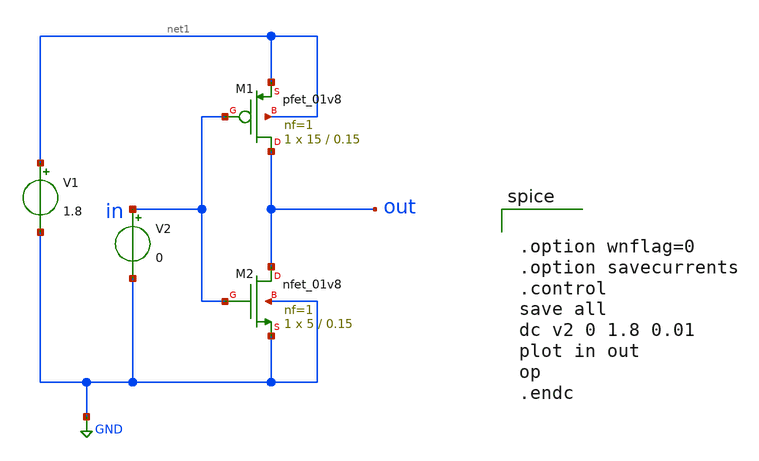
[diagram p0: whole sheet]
** sch_path: inverter_cmos.sch
**.subckt inverter_cmos
XM1 out in net1 net1 sky130_fd_pr__pfet_01v8 L=0.15 W=15 nf=1 ad='int((1 + 1)/2) * 15 / 1 * 0.29' as='int((1 + 2)/2) * 15 / 1 * 0.29'
+ pd='2*int((1 + 1)/2) * (15 / 1 + 0.29)' ps='2*int((1 + 2)/2) * (15 / 1 + 0.29)' nrd='0.29 / 15 ' nrs='0.29 / 15 '
+ sa=0 sb=0 sd=0 mult=1 m=1
XM2 out in GND GND sky130_fd_pr__nfet_01v8 L=0.15 W=5 nf=1 ad='int((1 + 1)/2) * 5 / 1 * 0.29' as='int((1 + 2)/2) * 5 / 1 * 0.29'
+ pd='2*int((1 + 1)/2) * (5 / 1 + 0.29)' ps='2*int((1 + 2)/2) * (5 / 1 + 0.29)' nrd='0.29 / 5 ' nrs='0.29 / 5 '
+ sa=0 sb=0 sd=0 mult=1 m=1
V1 net1 GND 1.8
V2 in GND 0
**** begin user architecture code
 .lib /foss/pdks/sky130A/libs.tech/combined/sky130.lib.spice tt

.param mc_mm_switch=0
.param mc_pr_switch=1



.option wnflag=0
.option savecurrents
.control
save all
dc v2 0 1.8 0.01
plot in out
op
.endc


**** end user architecture code
**.ends
.GLOBAL GND
.end
